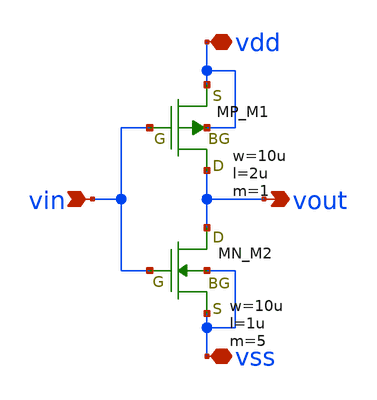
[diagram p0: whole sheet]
** sch_path: member_project/DCDC/ShuntaroOHNO/xschem/inverter_05v.sch
**.subckt inverter_05v vin vdd vss vout
*.ipin vin
*.iopin vdd
*.iopin vss
*.opin vout
XM1 vout vin vdd vdd PMOS w=10u l=2u as=0 ad=0 ps=0 pd=0 nrd=0 nrs=0 m=1
XM2 vout vin vss vss NMOS w=10u l=1u as=0 ad=0 ps=0 pd=0 nrd=0 nrs=0 m=5
**.ends
.end
